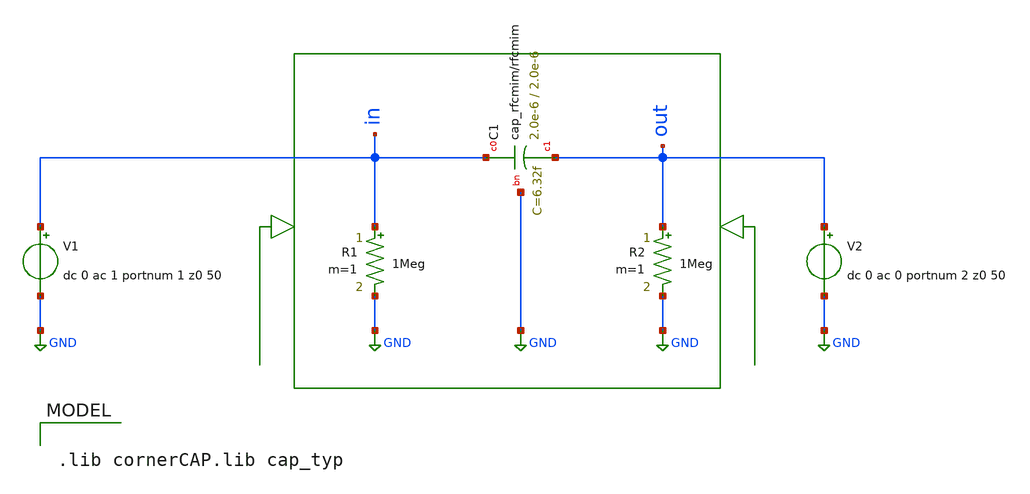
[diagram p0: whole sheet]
** sch_path: xschem/lc-vco/capacitors/rfcmim_tb.sch
**.subckt rfcmim_tb
R1 in GND 1Meg m=1
V1 in GND dc 0 ac 1 portnum 1 z0 50
R2 out GND 1Meg m=1
V2 out GND dc 0 ac 0 portnum 2 z0 50
XC1 in out GND cap_rfcmim w=2.0e-6 l=2.0e-6 wfeed=5.0e-6 m=1 mm_ok=1
**** begin user architecture code

.lib cornerCAP.lib cap_typ



.control

* Run S-parameter analysis: Linear sweep, 1 point, 2.44 GHz
sp lin 1 2.44G 2.44G

* Calculate C_diff and Q_diff
let C = 1/(2*PI*frequency*imag(1/Y_2_1))
print real(C)

.endc


**** end user architecture code
**.ends
.GLOBAL GND
.end
